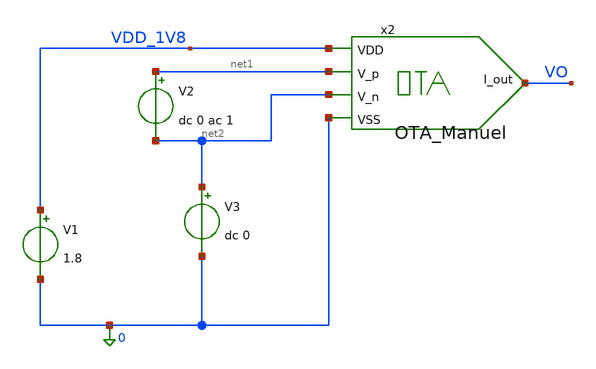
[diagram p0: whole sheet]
** sch_path: design/JNW_GR05_SKY130A/TB_JNWBIAS_OTA.sch
**.subckt TB_JNWBIAS_OTA
V1 VDD_1V8 0 1.8
V2 net1 net2 dc 0 ac 1
V3 net2 0 dc 0
x2 VDD_1V8 VO net2 net1 0 OTA_Manuel
**** begin user architecture code



* ngspice commands
.include tb_jnwbias_ota.cir



**** end user architecture code
**.ends
.end
